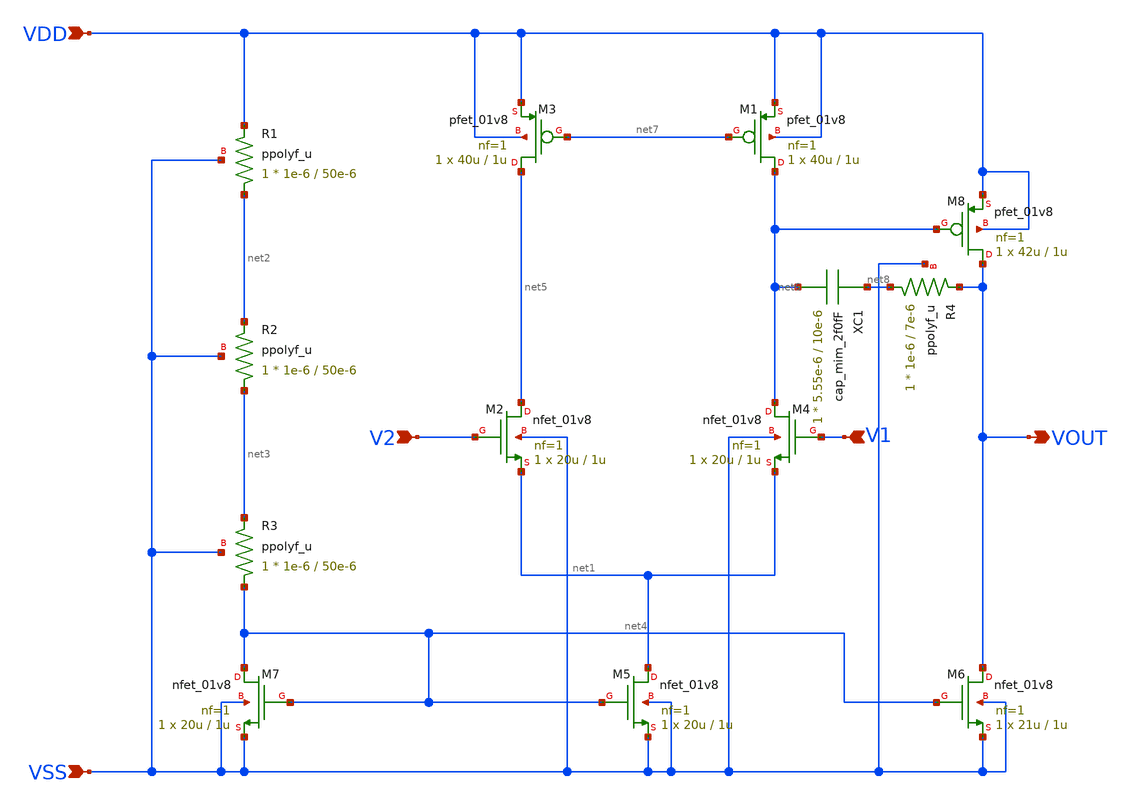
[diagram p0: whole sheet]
** sch_path: untitled.sch
**.subckt untitled VSS VDD V2 V1 VOUT
*.ipin VSS
*.ipin VDD
*.ipin V2
*.ipin V1
*.opin VOUT
XM2 net5 V2 net1 VSS sky130_fd_pr__nfet_01v8 L=1u W=20u nf=1 ad='int((nf+1)/2) * W/nf * 0.29' as='int((nf+2)/2) * W/nf * 0.29'
+ pd='2*int((nf+1)/2) * (W/nf + 0.29)' ps='2*int((nf+2)/2) * (W/nf + 0.29)' nrd='0.29 / W' nrs='0.29 / W'
+ sa=0 sb=0 sd=0 mult=1 m=1
XM1 net6 net7 VDD VDD sky130_fd_pr__pfet_01v8 L=1u W=40u nf=1 ad='int((nf+1)/2) * W/nf * 0.29' as='int((nf+2)/2) * W/nf * 0.29'
+ pd='2*int((nf+1)/2) * (W/nf + 0.29)' ps='2*int((nf+2)/2) * (W/nf + 0.29)' nrd='0.29 / W' nrs='0.29 / W'
+ sa=0 sb=0 sd=0 mult=1 m=1
XM4 net6 V1 net1 VSS sky130_fd_pr__nfet_01v8 L=1u W=20u nf=1 ad='int((nf+1)/2) * W/nf * 0.29' as='int((nf+2)/2) * W/nf * 0.29'
+ pd='2*int((nf+1)/2) * (W/nf + 0.29)' ps='2*int((nf+2)/2) * (W/nf + 0.29)' nrd='0.29 / W' nrs='0.29 / W'
+ sa=0 sb=0 sd=0 mult=1 m=1
XM5 net1 net4 VSS VSS sky130_fd_pr__nfet_01v8 L=1u W=20u nf=1 ad='int((nf+1)/2) * W/nf * 0.29' as='int((nf+2)/2) * W/nf * 0.29'
+ pd='2*int((nf+1)/2) * (W/nf + 0.29)' ps='2*int((nf+2)/2) * (W/nf + 0.29)' nrd='0.29 / W' nrs='0.29 / W'
+ sa=0 sb=0 sd=0 mult=1 m=1
XM6 VOUT net4 VSS VSS sky130_fd_pr__nfet_01v8 L=1u W=21u nf=1 ad='int((nf+1)/2) * W/nf * 0.29' as='int((nf+2)/2) * W/nf * 0.29'
+ pd='2*int((nf+1)/2) * (W/nf + 0.29)' ps='2*int((nf+2)/2) * (W/nf + 0.29)' nrd='0.29 / W' nrs='0.29 / W'
+ sa=0 sb=0 sd=0 mult=1 m=1
XM7 net4 net4 VSS VSS sky130_fd_pr__nfet_01v8 L=1u W=20u nf=1 ad='int((nf+1)/2) * W/nf * 0.29' as='int((nf+2)/2) * W/nf * 0.29'
+ pd='2*int((nf+1)/2) * (W/nf + 0.29)' ps='2*int((nf+2)/2) * (W/nf + 0.29)' nrd='0.29 / W' nrs='0.29 / W'
+ sa=0 sb=0 sd=0 mult=1 m=1
XR1 net2 VDD VSS ppolyf_u r_width=1e-6 r_length=50e-6 m=1
XR2 net3 net2 VSS ppolyf_u r_width=1e-6 r_length=50e-6 m=1
XR3 net4 net3 VSS ppolyf_u r_width=1e-6 r_length=50e-6 m=1
XM3 net5 net7 VDD VDD sky130_fd_pr__pfet_01v8 L=1u W=40u nf=1 ad='int((nf+1)/2) * W/nf * 0.29' as='int((nf+2)/2) * W/nf * 0.29'
+ pd='2*int((nf+1)/2) * (W/nf + 0.29)' ps='2*int((nf+2)/2) * (W/nf + 0.29)' nrd='0.29 / W' nrs='0.29 / W'
+ sa=0 sb=0 sd=0 mult=1 m=1
XM8 VOUT net6 VDD VDD sky130_fd_pr__pfet_01v8 L=1u W=42u nf=1 ad='int((nf+1)/2) * W/nf * 0.29' as='int((nf+2)/2) * W/nf * 0.29'
+ pd='2*int((nf+1)/2) * (W/nf + 0.29)' ps='2*int((nf+2)/2) * (W/nf + 0.29)' nrd='0.29 / W' nrs='0.29 / W'
+ sa=0 sb=0 sd=0 mult=1 m=1
XC1 net8 net6 cap_mim_2f0fF c_width=5.55e-6 c_length=10e-6 m=1
XR4 net8 VOUT VSS ppolyf_u r_width=1e-6 r_length=7e-6 m=1
**.ends
.end
